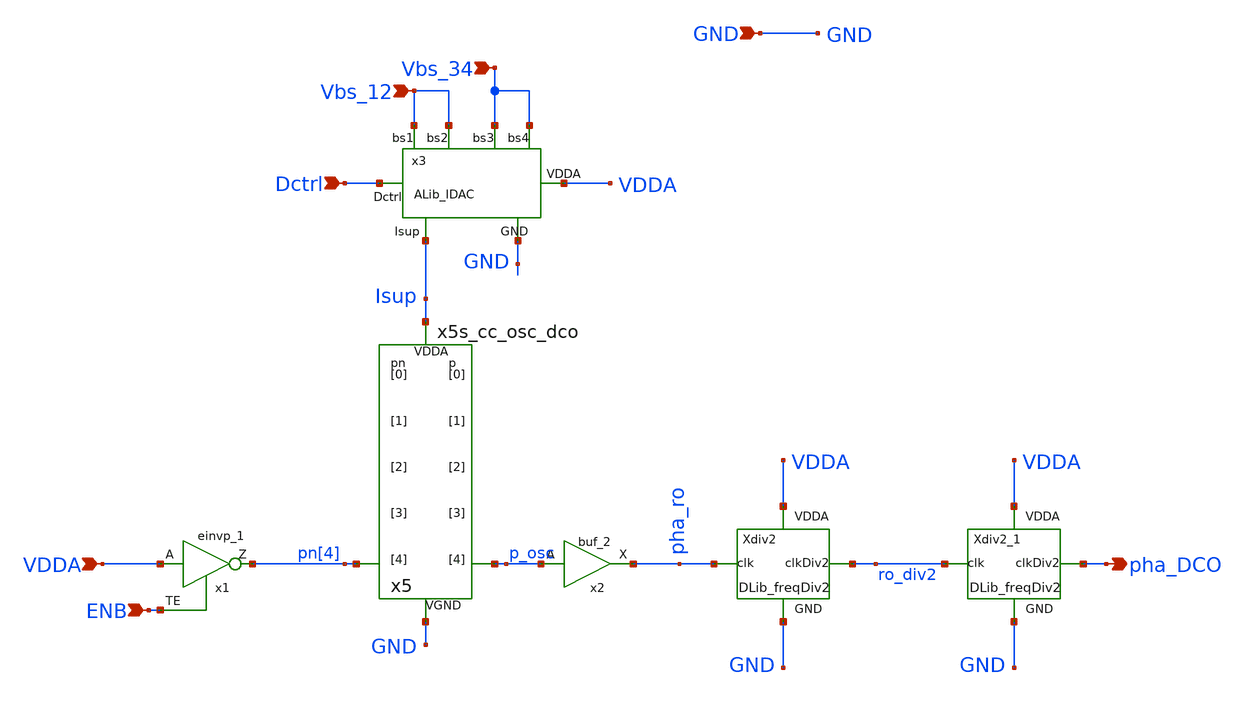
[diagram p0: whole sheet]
** sch_path: xschem/lib/ALib_DCO.sch
**.subckt ALib_DCO Dctrl Vbs_12 Vbs_34 pha_DCO ENB VDDA GND
*.ipin Dctrl
*.ipin Vbs_12
*.ipin Vbs_34
*.opin pha_DCO
*.ipin ENB
*.ipin VDDA
*.ipin GND
x1 VDDA ENB GND GND VDDA VDDA pn[4] sky130_fd_sc_hd__einvp_1
x2 p_osc GND GND VDDA VDDA pha_ro sky130_fd_sc_hd__buf_2
x3 Vbs_12 Vbs_12 Vbs_34 Vbs_34 Dctrl Isup VDDA GND ALib_IDAC
Xdiv2 pha_ro ro_div2 VDDA GND DLib_freqDiv2
Xdiv2_1 ro_div2 pha_DCO VDDA GND DLib_freqDiv2
x5 pn[4] p_osc Isup GND x5s_cc_osc_dco
**.ends

* expanding   symbol:  ../lib/ALib_IDAC.sym # of pins=8
** sym_path: xschem/lib/ALib_IDAC.sym
** sch_path: xschem/lib/ALib_IDAC.sch
.subckt ALib_IDAC Vbs1 Vbs2 Vbs3 Vbs4 Dctrl Isup VDDA GND
*.ipin Vbs3
*.ipin Vbs4
*.ipin Vbs1
*.ipin Vbs2
*.opin Isup
*.ipin Dctrl
*.ipin GND
*.ipin VDDA
x1 open GND GND VDDA VDDA lock sky130_fd_sc_hd__inv_2
XM1 net1 Vbs1 VDDA VDDA sky130_fd_pr__pfet_01v8_hvt L=0.5 W=1.8 nf=1 ad='int((1 + 1)/2) * 1.8 / 1 * 0.29'
+ as='int((1 + 2)/2) * 1.8 / 1 * 0.29' pd='2*int((1 + 1)/2) * (1.8 / 1 + 0.29)' ps='2*int((1 + 2)/2) * (1.8 / 1 + 0.29)'
+ nrd='0.29 / 1.8 ' nrs='0.29 / 1.8 ' sa=0 sb=0 sd=0 mult=1 m=1
XM2 Isup Vbs2 net1 net1 sky130_fd_pr__pfet_01v8_hvt L=0.5 W=1.8 nf=1 ad='int((1 + 1)/2) * 1.8 / 1 * 0.29'
+ as='int((1 + 2)/2) * 1.8 / 1 * 0.29' pd='2*int((1 + 1)/2) * (1.8 / 1 + 0.29)' ps='2*int((1 + 2)/2) * (1.8 / 1 + 0.29)'
+ nrd='0.29 / 1.8 ' nrs='0.29 / 1.8 ' sa=0 sb=0 sd=0 mult=1 m=1
x2 Dctrl GND GND VDDA VDDA open sky130_fd_sc_hd__buf_2
XM3 net2 Vbs3 VDDA VDDA sky130_fd_pr__pfet_01v8_hvt L=0.5 W=5.4 nf=3 ad='int((3 + 1)/2) * 5.4 / 3 * 0.29'
+ as='int((3 + 2)/2) * 5.4 / 3 * 0.29' pd='2*int((3 + 1)/2) * (5.4 / 3 + 0.29)' ps='2*int((3 + 2)/2) * (5.4 / 3 + 0.29)'
+ nrd='0.29 / 5.4 ' nrs='0.29 / 5.4 ' sa=0 sb=0 sd=0 mult=1 m=1
XM4 add_pwr Vbs4 net2 net2 sky130_fd_pr__pfet_01v8_hvt L=0.5 W=5.4 nf=3 ad='int((3 + 1)/2) * 5.4 / 3 * 0.29'
+ as='int((3 + 2)/2) * 5.4 / 3 * 0.29' pd='2*int((3 + 1)/2) * (5.4 / 3 + 0.29)' ps='2*int((3 + 2)/2) * (5.4 / 3 + 0.29)'
+ nrd='0.29 / 5.4 ' nrs='0.29 / 5.4 ' sa=0 sb=0 sd=0 mult=1 m=1
XM5 Isup lock add_pwr add_pwr sky130_fd_pr__pfet_01v8_hvt L=0.5 W=8 nf=2 ad='int((2 + 1)/2) * 8 / 2 * 0.29'
+ as='int((2 + 2)/2) * 8 / 2 * 0.29' pd='2*int((2 + 1)/2) * (8 / 2 + 0.29)' ps='2*int((2 + 2)/2) * (8 / 2 + 0.29)'
+ nrd='0.29 / 8 ' nrs='0.29 / 8 ' sa=0 sb=0 sd=0 mult=1 m=1
XM6 add_pwr open Isup GND sky130_fd_pr__nfet_01v8 L=0.5 W=4 nf=2 ad='int((nf+1)/2) * W/nf * 0.29' as='int((nf+2)/2) * W/nf * 0.29'
+ pd='2*int((nf+1)/2) * (W/nf + 0.29)' ps='2*int((nf+2)/2) * (W/nf + 0.29)' nrd='0.29 / W' nrs='0.29 / W'
+ sa=0 sb=0 sd=0 mult=1 m=1
XM7 input_R open add_pwr add_pwr sky130_fd_pr__pfet_01v8_hvt L=0.5 W=8 nf=2 ad='int((2 + 1)/2) * 8 / 2 * 0.29'
+ as='int((2 + 2)/2) * 8 / 2 * 0.29' pd='2*int((2 + 1)/2) * (8 / 2 + 0.29)' ps='2*int((2 + 2)/2) * (8 / 2 + 0.29)'
+ nrd='0.29 / 8 ' nrs='0.29 / 8 ' sa=0 sb=0 sd=0 mult=1 m=1
XM8 add_pwr lock input_R GND sky130_fd_pr__nfet_01v8 L=0.5 W=4 nf=2 ad='int((nf+1)/2) * W/nf * 0.29'
+ as='int((nf+2)/2) * W/nf * 0.29' pd='2*int((nf+1)/2) * (W/nf + 0.29)' ps='2*int((nf+2)/2) * (W/nf + 0.29)'
+ nrd='0.29 / W' nrs='0.29 / W' sa=0 sb=0 sd=0 mult=1 m=1
XR2 GND input_R GND sky130_fd_pr__res_xhigh_po_0p35 L=8.562 mult=1 m=1
.ends


* expanding   symbol:  ../lib/DLib_freqDiv2.sym # of pins=4
** sym_path: xschem/lib/DLib_freqDiv2.sym
** sch_path: xschem/lib/DLib_freqDiv2.sch
.subckt DLib_freqDiv2 clk clkDiv2 VDDA GND
*.opin clkDiv2
*.ipin clk
*.ipin VDDA
*.ipin GND
x1 clk D GND GND VDDA VDDA clkDiv2 Q_N sky130_fd_sc_hd__dfxbp_2
x2 clkinv Q_N_buf GND GND VDDA VDDA D sky130_fd_sc_hd__dfxtp_1
x3 clk GND GND VDDA VDDA clkinv sky130_fd_sc_hd__inv_4
x4 Q_N GND GND VDDA VDDA Q_N_buf sky130_fd_sc_hd__buf_4
.ends


* expanding   symbol:  x5s_cc_osc_dco.sym # of pins=4
** sym_path: xschem/lib/x5s_cc_osc_dco.sym
** sch_path: xschem/lib/x5s_cc_osc_dco.sch
.subckt x5s_cc_osc_dco pn[4] p[4] VDDA VGND
*.iopin VDDA
*.iopin VGND
*.opin p[4]
*.opin pn[4]
x1 VDDA net1 p[4] pn[4] net2 VGND cc_inv_dco
x2 VDDA net5 net1 net2 net8 VGND cc_inv_dco
x3 VDDA net3 net5 net8 net4 VGND cc_inv_dco
x4 VDDA net6 net3 net4 net7 VGND cc_inv_dco
x5 VDDA p[4] net6 net7 pn[4] VGND cc_inv_dco
.ends


* expanding   symbol:  ../lib/cc_inv_dco.sym # of pins=6
** sym_path: xschem/lib/cc_inv_dco.sym
** sch_path: xschem/lib/cc_inv_dco.sch
.subckt cc_inv_dco VDDA outp inp inn outn VGND
*.opin outp
*.ipin inn
*.iopin VGND
*.opin outn
*.ipin inp
*.iopin VDDA
x1 VDDA VGND outp inp main_inv_dco
x2 VPWR VGND outn inn main_inv_dco
x3 outp outn VDDA VGND aux_inv_dco
x4 outn outp VDDA VGND aux_inv_dco
.ends


* expanding   symbol:  ../lib/main_inv_dco.sym # of pins=4
** sym_path: xschem/lib/main_inv_dco.sym
** sch_path: xschem/lib/main_inv_dco.sch
.subckt main_inv_dco VDDA VGND Y A
*.iopin VDDA
*.iopin VGND
*.ipin A
*.opin Y
XM3 Y A VGND VGND sky130_fd_pr__nfet_01v8 L=1.2 W=4 nf=2 ad='int((nf+1)/2) * W/nf * 0.29' as='int((nf+2)/2) * W/nf * 0.29'
+ pd='2*int((nf+1)/2) * (W/nf + 0.29)' ps='2*int((nf+2)/2) * (W/nf + 0.29)' nrd='0.29 / W' nrs='0.29 / W'
+ sa=0 sb=0 sd=0 mult=1 m=1
XM2 Y A VDDA VDDA sky130_fd_pr__pfet_01v8 L=1.2 W=6 nf=2 ad='int((nf+1)/2) * W/nf * 0.29' as='int((nf+2)/2) * W/nf * 0.29'
+ pd='2*int((nf+1)/2) * (W/nf + 0.29)' ps='2*int((nf+2)/2) * (W/nf + 0.29)' nrd='0.29 / W' nrs='0.29 / W'
+ sa=0 sb=0 sd=0 mult=1 m=1
.ends


* expanding   symbol:  ../lib/aux_inv_dco.sym # of pins=4
** sym_path: xschem/lib/aux_inv_dco.sym
** sch_path: xschem/lib/aux_inv_dco.sch
.subckt aux_inv_dco A Y VDDA VGND
*.iopin VDDA
*.iopin VGND
*.ipin A
*.opin Y
XM3 Y A VGND VGND sky130_fd_pr__nfet_01v8 L=1.2 W=2 nf=1 ad='int((nf+1)/2) * W/nf * 0.29' as='int((nf+2)/2) * W/nf * 0.29'
+ pd='2*int((nf+1)/2) * (W/nf + 0.29)' ps='2*int((nf+2)/2) * (W/nf + 0.29)' nrd='0.29 / W' nrs='0.29 / W'
+ sa=0 sb=0 sd=0 mult=1 m=1
XM2 Y A VDDA VDDA sky130_fd_pr__pfet_01v8 L=1.2 W=3 nf=1 ad='int((nf+1)/2) * W/nf * 0.29' as='int((nf+2)/2) * W/nf * 0.29'
+ pd='2*int((nf+1)/2) * (W/nf + 0.29)' ps='2*int((nf+2)/2) * (W/nf + 0.29)' nrd='0.29 / W' nrs='0.29 / W'
+ sa=0 sb=0 sd=0 mult=1 m=1
.ends

.end
